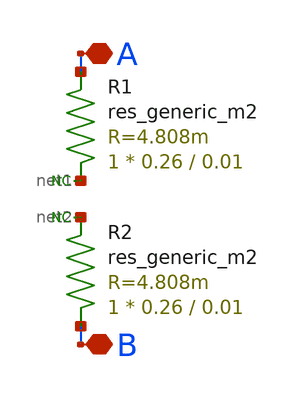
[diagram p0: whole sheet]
** sch_path: common/tk_em2o.sch
* Copyright 2023 David Mitchell Bailey
* Licensed under the Apache License, Version 2.0 (the "License");
* you may not use this file except in compliance with the License.
* You may obtain a copy of the License at
* https://www.apache.org/licenses/LICENSE-2.0
* Unless required by applicable law or agreed to in writing, software
* distributed under the License is distributed on an "AS IS" BASIS,
* WITHOUT WARRANTIES OR CONDITIONS OF ANY KIND, either express or implied.
* See the License for the specific language governing permissions and
* limitations under the License.
**.subckt tk_em2o A B
*.iopin A
*.iopin B
R1 net1 A sky130_fd_pr__res_generic_m2 W=0.26 L=0.01 m=1
R2 B net2 sky130_fd_pr__res_generic_m2 W=0.26 L=0.01 m=1
* noconn #net1
* noconn #net2
**.ends
.end
